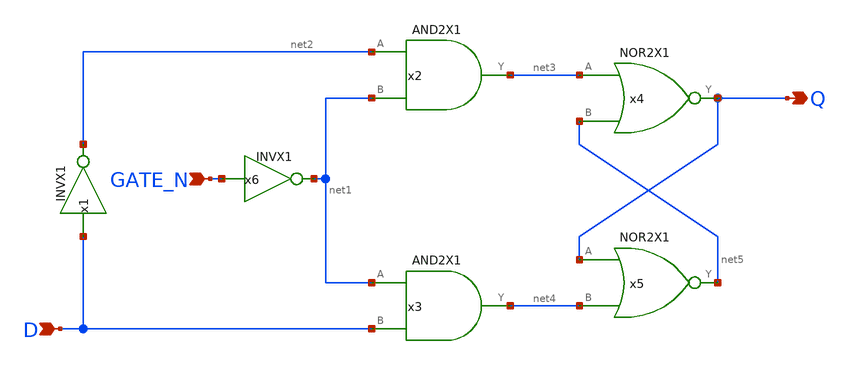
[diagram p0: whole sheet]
** sch_path: current/xschem/DLATCHN.sch
**.subckt DLATCHN Q D GATE_N
*.opin Q
*.ipin D
*.ipin GATE_N
x1 net2 D VDD VSS INVX1
x2 net3 net2 net1 VDD VSS AND2X1
x3 net4 net1 D VDD VSS AND2X1
x4 Q net3 net5 VDD VSS NOR2X1
x5 net5 Q net4 VDD VSS NOR2X1
x6 net1 GATE_N VDD VSS INVX1
**.ends
.end
